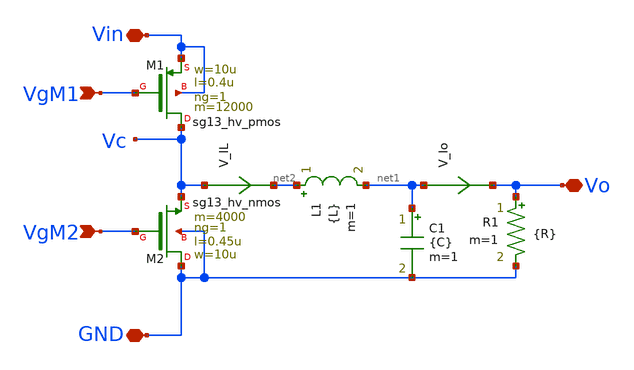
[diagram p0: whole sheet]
** sch_path: xschem/IHP_Tapeout24_AMsent20241028/DCDC_Buck_V2.sch
**.subckt DCDC_Buck_V2 Vin VgM1 VgM2 Vo GND
*.iopin Vin
*.ipin VgM1
*.ipin VgM2
*.iopin Vo
*.iopin GND
XM2 GND VgM2 Vc GND sg13_hv_nmos w=10u l=0.45u ng=1 m=4000 mm_ok=1
XM1 Vc VgM1 Vin Vin sg13_hv_pmos w=10u l=0.4u ng=1 m=12000 mm_ok=1
L1 net2 net1 {L} m=1
C1 net1 GND {C} m=1
V_Io net1 Vo 0
.save i(v_io)
V_IL Vc net2 0
.save i(v_il)
R1 Vo GND {R} m=1
**.ends
.end
